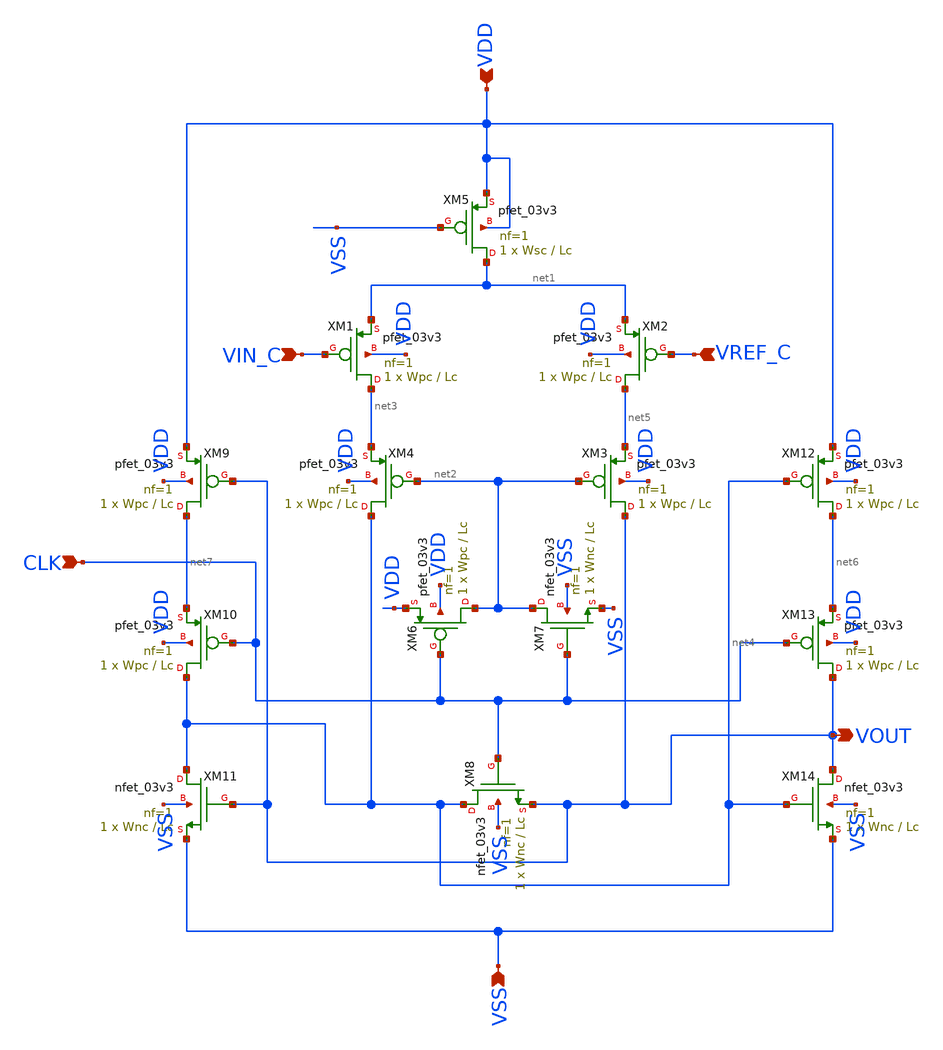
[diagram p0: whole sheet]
** sch_path: src/schematics/latched_comparator/COMPARATOR_SD.sch
**.subckt COMPARATOR_SD VIN_C VREF_C CLK VOUT VDD VSS
*.ipin VIN_C
*.ipin VREF_C
*.ipin CLK
*.opin VOUT
*.ipin VDD
*.ipin VSS
XM1 net3 VIN_C net1 VDD pfet_03v3 L=Lc W=Wpc nf=1 ad='int((nf+1)/2) * W/nf * 0.18u' as='int((nf+2)/2) * W/nf * 0.18u'
+ pd='2*int((nf+1)/2) * (W/nf + 0.18u)' ps='2*int((nf+2)/2) * (W/nf + 0.18u)' nrd='0.18u / W' nrs='0.18u / W'
+ sa=0 sb=0 sd=0 m=1
XM2 net5 VREF_C net1 VDD pfet_03v3 L=Lc W=Wpc nf=1 ad='int((nf+1)/2) * W/nf * 0.18u' as='int((nf+2)/2) * W/nf * 0.18u'
+ pd='2*int((nf+1)/2) * (W/nf + 0.18u)' ps='2*int((nf+2)/2) * (W/nf + 0.18u)' nrd='0.18u / W' nrs='0.18u / W'
+ sa=0 sb=0 sd=0 m=1
XM3 VOUT net2 net5 VDD pfet_03v3 L=Lc W=Wpc nf=1 ad='int((nf+1)/2) * W/nf * 0.18u' as='int((nf+2)/2) * W/nf * 0.18u'
+ pd='2*int((nf+1)/2) * (W/nf + 0.18u)' ps='2*int((nf+2)/2) * (W/nf + 0.18u)' nrd='0.18u / W' nrs='0.18u / W'
+ sa=0 sb=0 sd=0 m=1
XM4 net4 net2 net3 VDD pfet_03v3 L=Lc W=Wpc nf=1 ad='int((nf+1)/2) * W/nf * 0.18u' as='int((nf+2)/2) * W/nf * 0.18u'
+ pd='2*int((nf+1)/2) * (W/nf + 0.18u)' ps='2*int((nf+2)/2) * (W/nf + 0.18u)' nrd='0.18u / W' nrs='0.18u / W'
+ sa=0 sb=0 sd=0 m=1
XM6 net2 CLK VDD VDD pfet_03v3 L=Lc W=Wpc nf=1 ad='int((nf+1)/2) * W/nf * 0.18u' as='int((nf+2)/2) * W/nf * 0.18u'
+ pd='2*int((nf+1)/2) * (W/nf + 0.18u)' ps='2*int((nf+2)/2) * (W/nf + 0.18u)' nrd='0.18u / W' nrs='0.18u / W'
+ sa=0 sb=0 sd=0 m=1
XM7 net2 CLK VSS VSS nfet_03v3 L=Lc W=Wnc nf=1 ad='int((nf+1)/2) * W/nf * 0.18u' as='int((nf+2)/2) * W/nf * 0.18u'
+ pd='2*int((nf+1)/2) * (W/nf + 0.18u)' ps='2*int((nf+2)/2) * (W/nf + 0.18u)' nrd='0.18u / W' nrs='0.18u / W'
+ sa=0 sb=0 sd=0 m=1
XM8 net4 CLK VOUT VSS nfet_03v3 L=Lc W=Wnc nf=1 ad='int((nf+1)/2) * W/nf * 0.18u' as='int((nf+2)/2) * W/nf * 0.18u'
+ pd='2*int((nf+1)/2) * (W/nf + 0.18u)' ps='2*int((nf+2)/2) * (W/nf + 0.18u)' nrd='0.18u / W' nrs='0.18u / W'
+ sa=0 sb=0 sd=0 m=1
XM9 net7 VOUT VDD VDD pfet_03v3 L=Lc W=Wpc nf=1 ad='int((nf+1)/2) * W/nf * 0.18u' as='int((nf+2)/2) * W/nf * 0.18u'
+ pd='2*int((nf+1)/2) * (W/nf + 0.18u)' ps='2*int((nf+2)/2) * (W/nf + 0.18u)' nrd='0.18u / W' nrs='0.18u / W'
+ sa=0 sb=0 sd=0 m=1
XM10 net4 CLK net7 VDD pfet_03v3 L=Lc W=Wpc nf=1 ad='int((nf+1)/2) * W/nf * 0.18u' as='int((nf+2)/2) * W/nf * 0.18u'
+ pd='2*int((nf+1)/2) * (W/nf + 0.18u)' ps='2*int((nf+2)/2) * (W/nf + 0.18u)' nrd='0.18u / W' nrs='0.18u / W'
+ sa=0 sb=0 sd=0 m=1
XM11 net4 VOUT VSS VSS nfet_03v3 L=Lc W=Wnc nf=1 ad='int((nf+1)/2) * W/nf * 0.18u' as='int((nf+2)/2) * W/nf * 0.18u'
+ pd='2*int((nf+1)/2) * (W/nf + 0.18u)' ps='2*int((nf+2)/2) * (W/nf + 0.18u)' nrd='0.18u / W' nrs='0.18u / W'
+ sa=0 sb=0 sd=0 m=1
XM12 net6 net4 VDD VDD pfet_03v3 L=Lc W=Wpc nf=1 ad='int((nf+1)/2) * W/nf * 0.18u' as='int((nf+2)/2) * W/nf * 0.18u'
+ pd='2*int((nf+1)/2) * (W/nf + 0.18u)' ps='2*int((nf+2)/2) * (W/nf + 0.18u)' nrd='0.18u / W' nrs='0.18u / W'
+ sa=0 sb=0 sd=0 m=1
XM13 VOUT CLK net6 VDD pfet_03v3 L=Lc W=Wpc nf=1 ad='int((nf+1)/2) * W/nf * 0.18u' as='int((nf+2)/2) * W/nf * 0.18u'
+ pd='2*int((nf+1)/2) * (W/nf + 0.18u)' ps='2*int((nf+2)/2) * (W/nf + 0.18u)' nrd='0.18u / W' nrs='0.18u / W'
+ sa=0 sb=0 sd=0 m=1
XM14 VOUT net4 VSS VSS nfet_03v3 L=Lc W=Wnc nf=1 ad='int((nf+1)/2) * W/nf * 0.18u' as='int((nf+2)/2) * W/nf * 0.18u'
+ pd='2*int((nf+1)/2) * (W/nf + 0.18u)' ps='2*int((nf+2)/2) * (W/nf + 0.18u)' nrd='0.18u / W' nrs='0.18u / W'
+ sa=0 sb=0 sd=0 m=1
XM5 net1 VSS VDD VDD pfet_03v3 L=Lc W=Wsc nf=1 ad='int((nf+1)/2) * W/nf * 0.18u' as='int((nf+2)/2) * W/nf * 0.18u'
+ pd='2*int((nf+1)/2) * (W/nf + 0.18u)' ps='2*int((nf+2)/2) * (W/nf + 0.18u)' nrd='0.18u / W' nrs='0.18u / W'
+ sa=0 sb=0 sd=0 m=1
**.ends
.end
